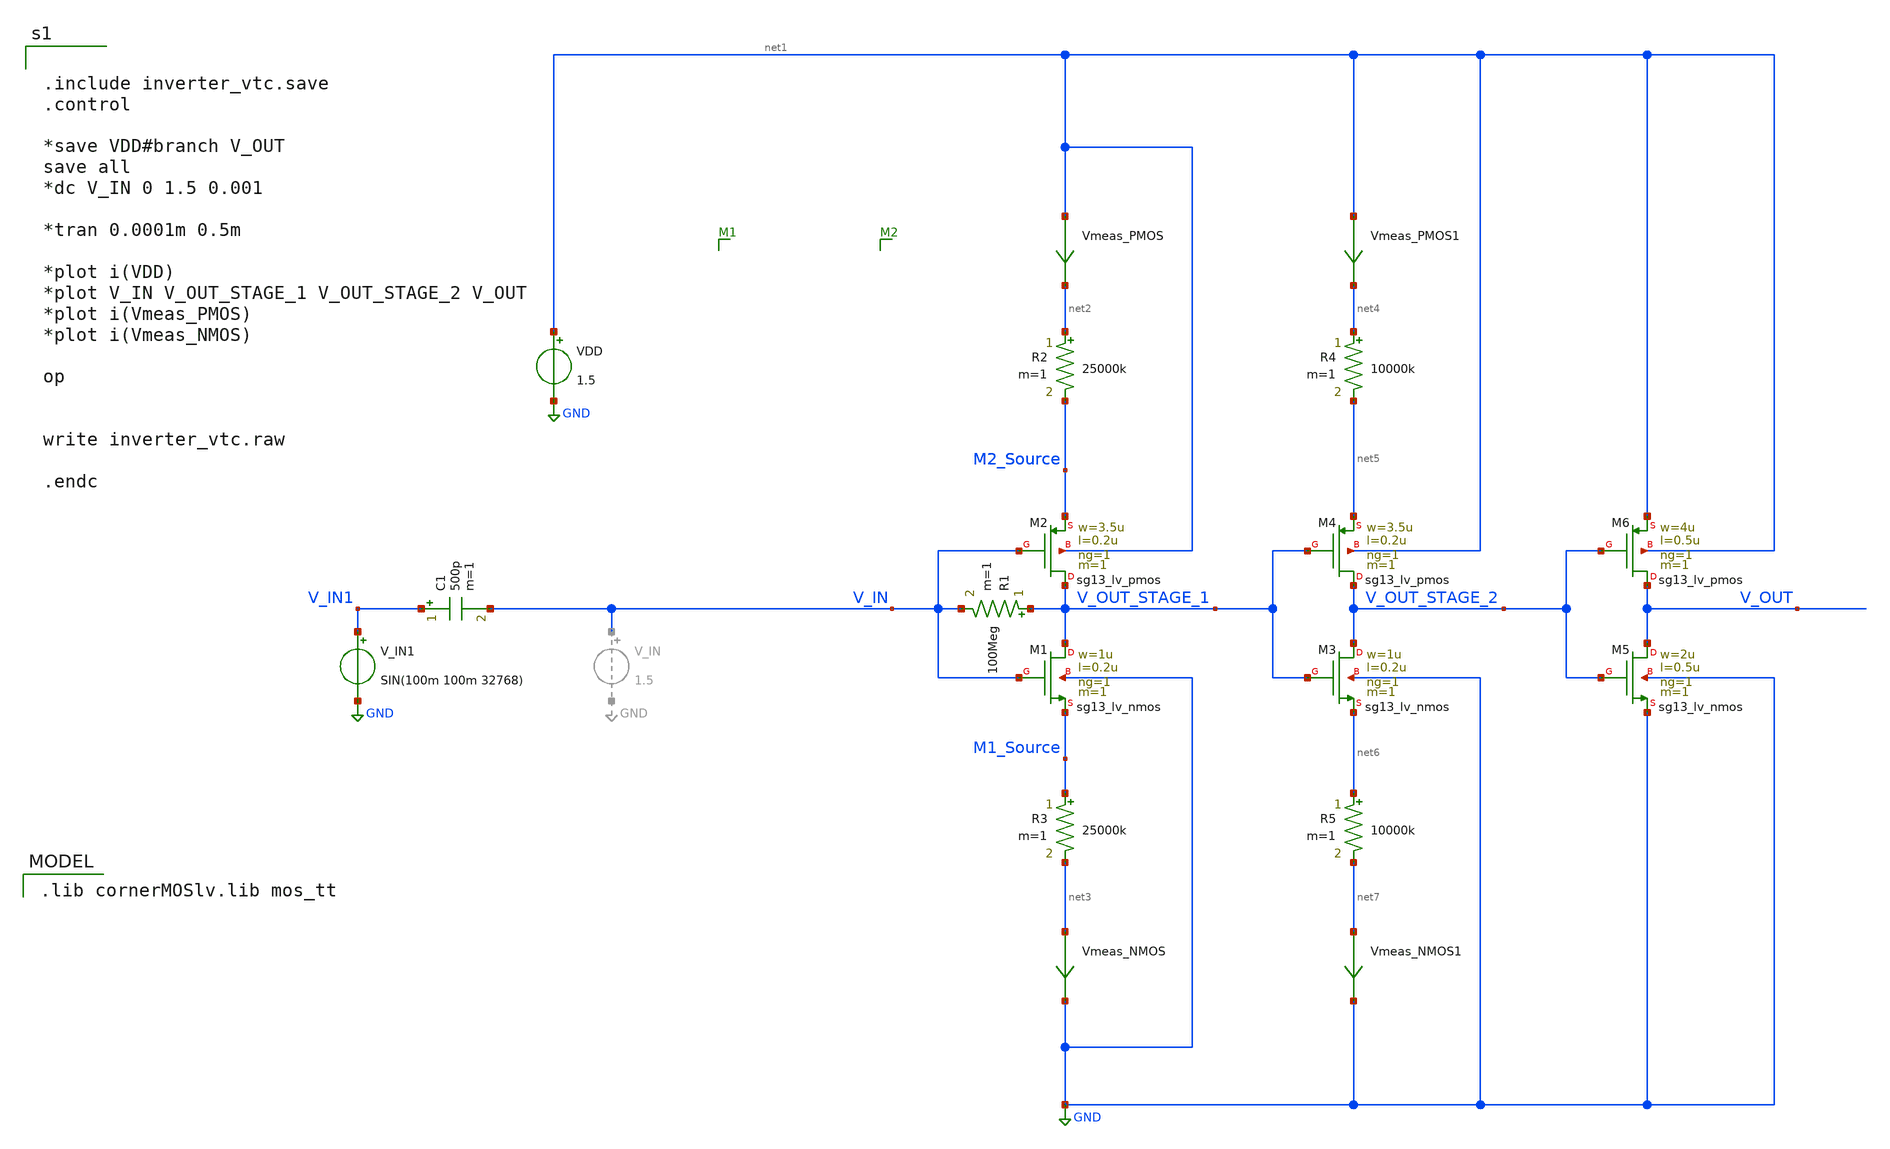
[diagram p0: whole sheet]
** sch_path: inverter_vtc.sch
**.subckt inverter_vtc
XM1 V_OUT_STAGE_1 V_IN M1_Source GND sg13_lv_nmos w=1u l=0.2u ng=1 m=1 mm_ok=1
XM2 V_OUT_STAGE_1 V_IN M2_Source net1 sg13_lv_pmos w=3.5u l=0.2u ng=1 m=1 mm_ok=1
Vmeas_NMOS net3 GND 0
.save i(vmeas_nmos)
Vmeas_PMOS net1 net2 0
.save i(vmeas_pmos)
VDD net1 GND 1.5
R1 V_OUT_STAGE_1 V_IN 100Meg m=1
R2 net2 M2_Source 25000k m=1
R3 M1_Source net3 25000k m=1
V_IN1 V_IN1 GND SIN(100m 100m 32768)
C1 V_IN1 V_IN 500p m=1
XM3 V_OUT_STAGE_2 V_OUT_STAGE_1 net6 GND sg13_lv_nmos w=1u l=0.2u ng=1 m=1 mm_ok=1
XM4 V_OUT_STAGE_2 V_OUT_STAGE_1 net5 net1 sg13_lv_pmos w=3.5u l=0.2u ng=1 m=1 mm_ok=1
Vmeas_NMOS1 net7 GND 0
.save i(vmeas_nmos1)
Vmeas_PMOS1 net1 net4 0
.save i(vmeas_pmos1)
R4 net4 net5 10000k m=1
R5 net6 net7 10000k m=1
XM5 V_OUT V_OUT_STAGE_2 GND GND sg13_lv_nmos w=2u l=0.5u ng=1 m=1 mm_ok=1
XM6 V_OUT V_OUT_STAGE_2 net1 net1 sg13_lv_pmos w=4u l=0.5u ng=1 m=1 mm_ok=1
**** begin user architecture code
 .lib cornerMOSlv.lib mos_tt



.include inverter_vtc.save
.control

*save VDD#branch V_OUT
save all
*dc V_IN 0 1.5 0.001

*tran 0.0001m 0.5m

*plot i(VDD)
*plot V_IN V_OUT_STAGE_1 V_OUT_STAGE_2 V_OUT
*plot i(Vmeas_PMOS)
*plot i(Vmeas_NMOS)

op


write inverter_vtc.raw

.endc


**** end user architecture code
**.ends
.GLOBAL GND
.end
